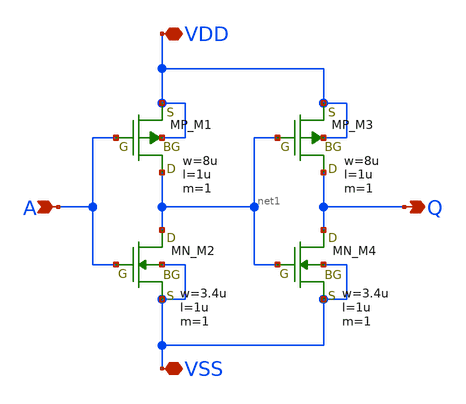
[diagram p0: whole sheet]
** sch_path: member_project/inverter/RISE-A/WEI_YICHENG/inverter_wei_Rev2.sch
**.subckt inverter_wei_Rev2 Q A VDD VSS
*.opin Q
*.ipin A
*.iopin VDD
*.iopin VSS
XM1 net1 A VDD VDD PMOS w=8u l=1u nrd=0 nrs=0 m=1
XM2 net1 A VSS VSS NMOS w=3.4u l=1u nrd=0 nrs=0 m=1
XM3 Q net1 VDD VDD PMOS w=8u l=1u nrd=0 nrs=0 m=1
XM4 Q net1 VSS VSS NMOS w=3.4u l=1u nrd=0 nrs=0 m=1
**.ends
.end
